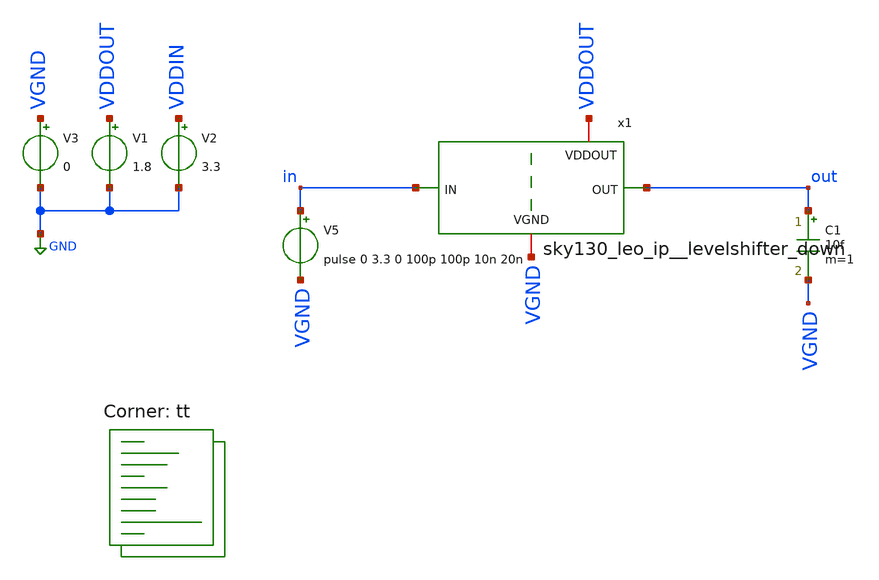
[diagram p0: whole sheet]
** sch_path: tt_um_tt08_aicd_playground/dependencies/sky130_leo_ip__levelshifter/xschem/sky130_leo_ip__levelshifter_down_tb.sch
**.subckt sky130_leo_ip__levelshifter_down_tb
x1 VDDOUT out in VGND sky130_leo_ip__levelshifter_down
V1 VDDOUT GND 1.8
V2 VDDIN GND 3.3
V3 VGND GND 0
C1 out VGND 10f m=1
V5 in VGND pulse 0 3.3 0 100p 100p 10n 20n
**** begin user architecture code
.lib $::SKYWATER_MODELS/sky130.lib.spice tt



.param vddin = 1.8
.param vddout = 3.3

*.include {DUT_path}

.control
    save all

    *** ADD SAVE LINES HERE -- TEMPLATE for NMOS M1 and PMOS M2 given below, copy and adjust device
+ name
    *save @m.x1.xm1.msky130_fd_pr__nfet_01v8_lvt[id] @m.x1.xm1.msky130_fd_pr__nfet_01v8_lvt[gm]
+ @m.x1.xm1.msky130_fd_pr__nfet_01v8_lvt[gds]
    *save @m.x1.xm2.msky130_fd_pr__pfet_01v8_lvt[id] @m.x1.xm2.msky130_fd_pr__pfet_01v8_lvt[gm]
+ @m.x1.xm2.msky130_fd_pr__pfet_01v8_lvt[gds]

    * operating point
    op
    write tb.raw
    set appendwrite

    * transient simulation
    options method=gear
    tran 1p 40n
    save all
    write tb.raw

    * measure parameters

    * get the peak-to-peak voltage
    meas TRAN range PP v(out)
    let ten=0.1*range
    let ninety=0.9*range

    print range ten ninety

    # rise and fall time
    meas TRAN rise_time TRIG v(out) VAL=ten    TD=0ns  RISE=1   TARG v(out) VAL=ninety TD=0ns
+  RISE=1
    meas TRAN fall_time TRIG v(out) VAL=ninety TD=5ns  FALL=1   TARG v(out) VAL=TEN    TD=5ns
+  FALL=1

    print rise_time fall_time

    *echo $&ugf > {simpath}/{filename}_{N}.data

.endc



**** end user architecture code
**.ends

* expanding   symbol:  sky130_leo_ip__levelshifter_down.sym # of pins=4
** sym_path: tt_um_tt08_aicd_playground/dependencies/sky130_leo_ip__levelshifter/xschem/sky130_leo_ip__levelshifter_down.sym
** sch_path: tt_um_tt08_aicd_playground/dependencies/sky130_leo_ip__levelshifter/xschem/sky130_leo_ip__levelshifter_down.sch
.subckt sky130_leo_ip__levelshifter_down VDDOUT OUT IN VGND
*.ipin IN
*.iopin VGND
*.opin OUT
*.iopin VDDOUT
XM3 OUT n VGND VGND sky130_fd_pr__nfet_01v8 L=0.15 W=0.42 nf=1 ad='int((nf+1)/2) * W/nf * 0.29' as='int((nf+2)/2) * W/nf * 0.29'
+ pd='2*int((nf+1)/2) * (W/nf + 0.29)' ps='2*int((nf+2)/2) * (W/nf + 0.29)' nrd='0.29 / W' nrs='0.29 / W'
+ sa=0 sb=0 sd=0 mult=1 m=1
XM4 OUT n VDDOUT VDDOUT sky130_fd_pr__pfet_01v8 L=0.15 W=1 nf=1 ad='int((nf+1)/2) * W/nf * 0.29' as='int((nf+2)/2) * W/nf * 0.29'
+ pd='2*int((nf+1)/2) * (W/nf + 0.29)' ps='2*int((nf+2)/2) * (W/nf + 0.29)' nrd='0.29 / W' nrs='0.29 / W'
+ sa=0 sb=0 sd=0 mult=1 m=1
XM5 n IN VDDOUT VDDOUT sky130_fd_pr__pfet_g5v0d10v5 L=0.5 W=0.42 nf=1 ad='int((nf+1)/2) * W/nf * 0.29'
+ as='int((nf+2)/2) * W/nf * 0.29' pd='2*int((nf+1)/2) * (W/nf + 0.29)' ps='2*int((nf+2)/2) * (W/nf + 0.29)'
+ nrd='0.29 / W' nrs='0.29 / W' sa=0 sb=0 sd=0 mult=1 m=1
XM6 n IN VGND VGND sky130_fd_pr__nfet_g5v0d10v5 L=0.5 W=1 nf=1 ad='int((nf+1)/2) * W/nf * 0.29' as='int((nf+2)/2) * W/nf * 0.29'
+ pd='2*int((nf+1)/2) * (W/nf + 0.29)' ps='2*int((nf+2)/2) * (W/nf + 0.29)' nrd='0.29 / W' nrs='0.29 / W'
+ sa=0 sb=0 sd=0 mult=1 m=1
.ends

.GLOBAL GND
.end
